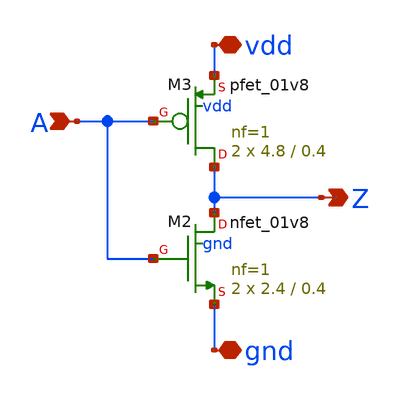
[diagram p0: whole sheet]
** sch_path: sram_2_64_scn4m/pinv_14.sch
**.subckt pinv_14 A Z vdd gnd
*.ipin A
*.opin Z
*.iopin vdd
*.iopin gnd
XM2 Z A gnd gnd sky130_fd_pr__nfet_01v8 L=0.4 W=2.4 nf=1 ad='int((nf+1)/2) * W/nf * 0.29' as='int((nf+2)/2) * W/nf * 0.29'
+ pd='2*int((nf+1)/2) * (W/nf + 0.29)' ps='2*int((nf+2)/2) * (W/nf + 0.29)' nrd='0.29 / W' nrs='0.29 / W'
+ sa=0 sb=0 sd=0 mult=2 m=2
XM3 Z A vdd vdd sky130_fd_pr__pfet_01v8 L=0.4 W=4.8 nf=1 ad='int((nf+1)/2) * W/nf * 0.29' as='int((nf+2)/2) * W/nf * 0.29'
+ pd='2*int((nf+1)/2) * (W/nf + 0.29)' ps='2*int((nf+2)/2) * (W/nf + 0.29)' nrd='0.29 / W' nrs='0.29 / W'
+ sa=0 sb=0 sd=0 mult=2 m=2
**.ends
.end
